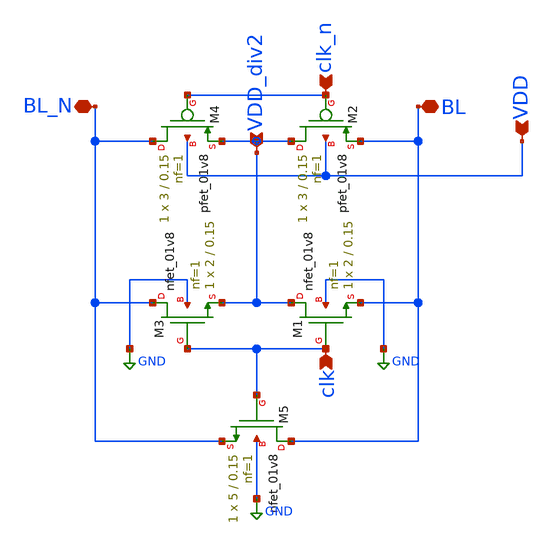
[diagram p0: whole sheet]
** sch_path: analog/schematics/precharge_trans_gate.sch
**.subckt precharge_trans_gate VDD_div2 clk_n clk BL BL_N VDD
*.ipin VDD_div2
*.ipin clk_n
*.ipin clk
*.iopin BL
*.iopin BL_N
*.ipin VDD
XM1 VDD_div2 clk BL GND sky130_fd_pr__nfet_01v8 L=0.15 W=2 nf=1 ad='int((nf+1)/2) * W/nf * 0.29' as='int((nf+2)/2) * W/nf * 0.29'
+ pd='2*int((nf+1)/2) * (W/nf + 0.29)' ps='2*int((nf+2)/2) * (W/nf + 0.29)' nrd='0.29 / W' nrs='0.29 / W'
+ sa=0 sb=0 sd=0 mult=1 m=1
XM3 BL_N clk VDD_div2 GND sky130_fd_pr__nfet_01v8 L=0.15 W=2 nf=1 ad='int((nf+1)/2) * W/nf * 0.29' as='int((nf+2)/2) * W/nf * 0.29'
+ pd='2*int((nf+1)/2) * (W/nf + 0.29)' ps='2*int((nf+2)/2) * (W/nf + 0.29)' nrd='0.29 / W' nrs='0.29 / W'
+ sa=0 sb=0 sd=0 mult=1 m=1
XM2 VDD_div2 clk_n BL VDD sky130_fd_pr__pfet_01v8 L=0.15 W=3 nf=1 ad='int((nf+1)/2) * W/nf * 0.29' as='int((nf+2)/2) * W/nf * 0.29'
+ pd='2*int((nf+1)/2) * (W/nf + 0.29)' ps='2*int((nf+2)/2) * (W/nf + 0.29)' nrd='0.29 / W' nrs='0.29 / W'
+ sa=0 sb=0 sd=0 mult=1 m=1
XM4 BL_N clk_n VDD_div2 VDD sky130_fd_pr__pfet_01v8 L=0.15 W=3 nf=1 ad='int((nf+1)/2) * W/nf * 0.29'
+ as='int((nf+2)/2) * W/nf * 0.29' pd='2*int((nf+1)/2) * (W/nf + 0.29)' ps='2*int((nf+2)/2) * (W/nf + 0.29)'
+ nrd='0.29 / W' nrs='0.29 / W' sa=0 sb=0 sd=0 mult=1 m=1
XM5 BL clk BL_N GND sky130_fd_pr__nfet_01v8 L=0.15 W=5 nf=1 ad='int((nf+1)/2) * W/nf * 0.29' as='int((nf+2)/2) * W/nf * 0.29'
+ pd='2*int((nf+1)/2) * (W/nf + 0.29)' ps='2*int((nf+2)/2) * (W/nf + 0.29)' nrd='0.29 / W' nrs='0.29 / W'
+ sa=0 sb=0 sd=0 mult=1 m=1
**.ends
.GLOBAL GND
.end
